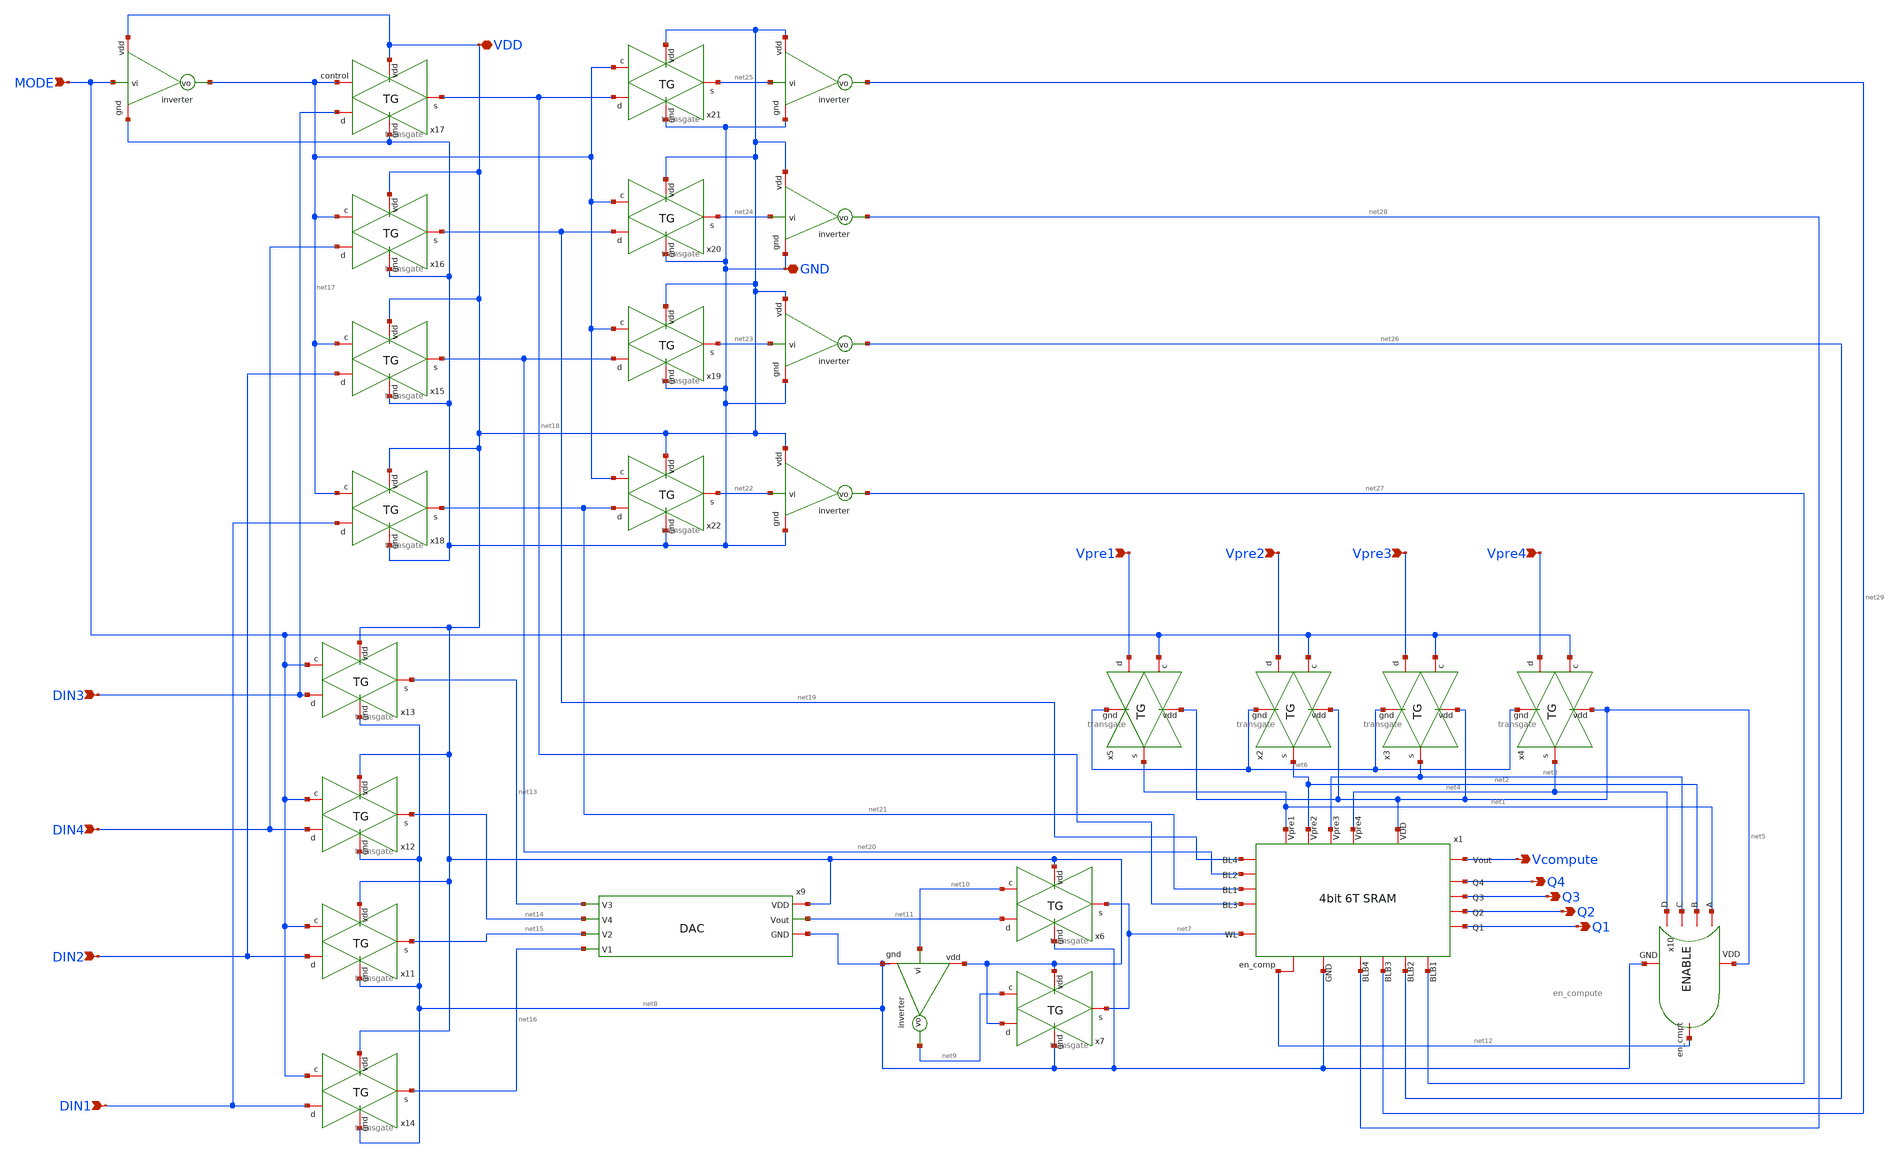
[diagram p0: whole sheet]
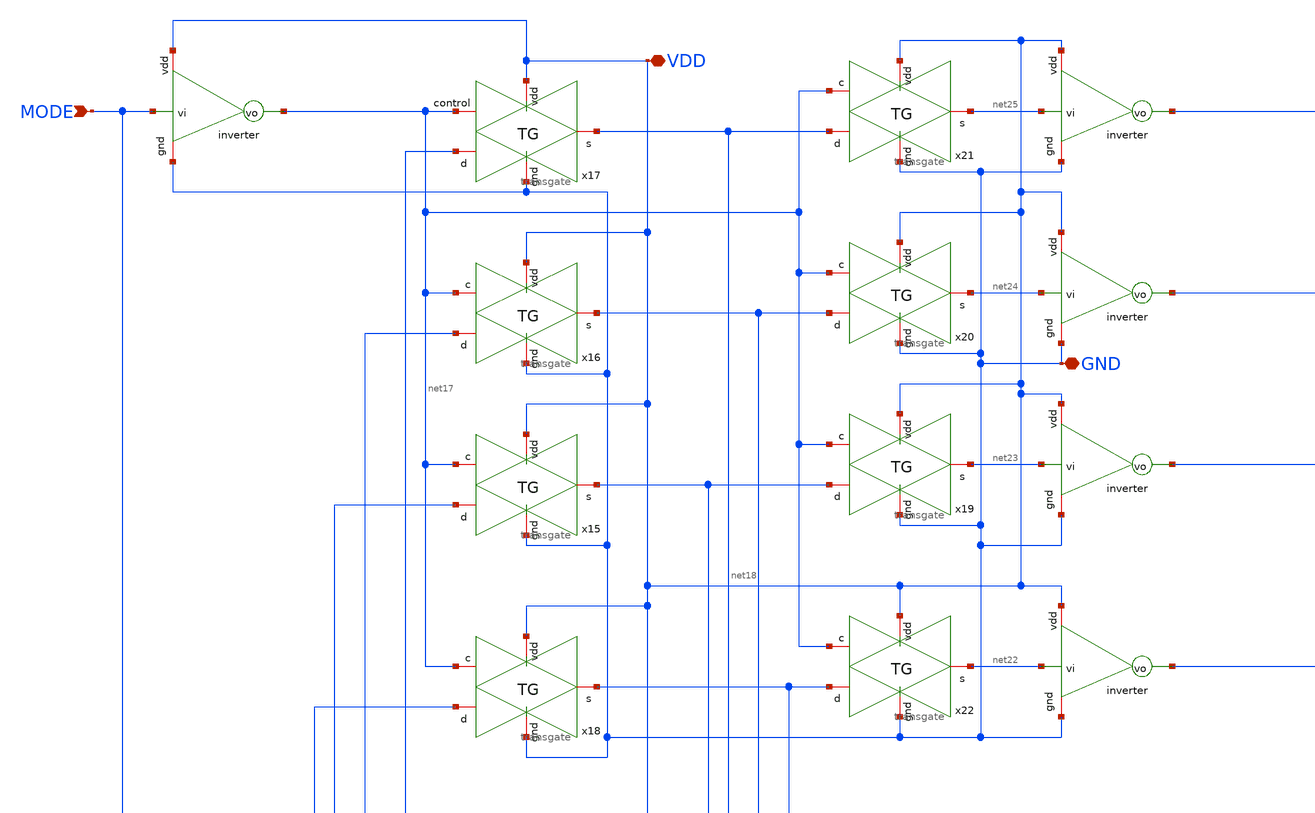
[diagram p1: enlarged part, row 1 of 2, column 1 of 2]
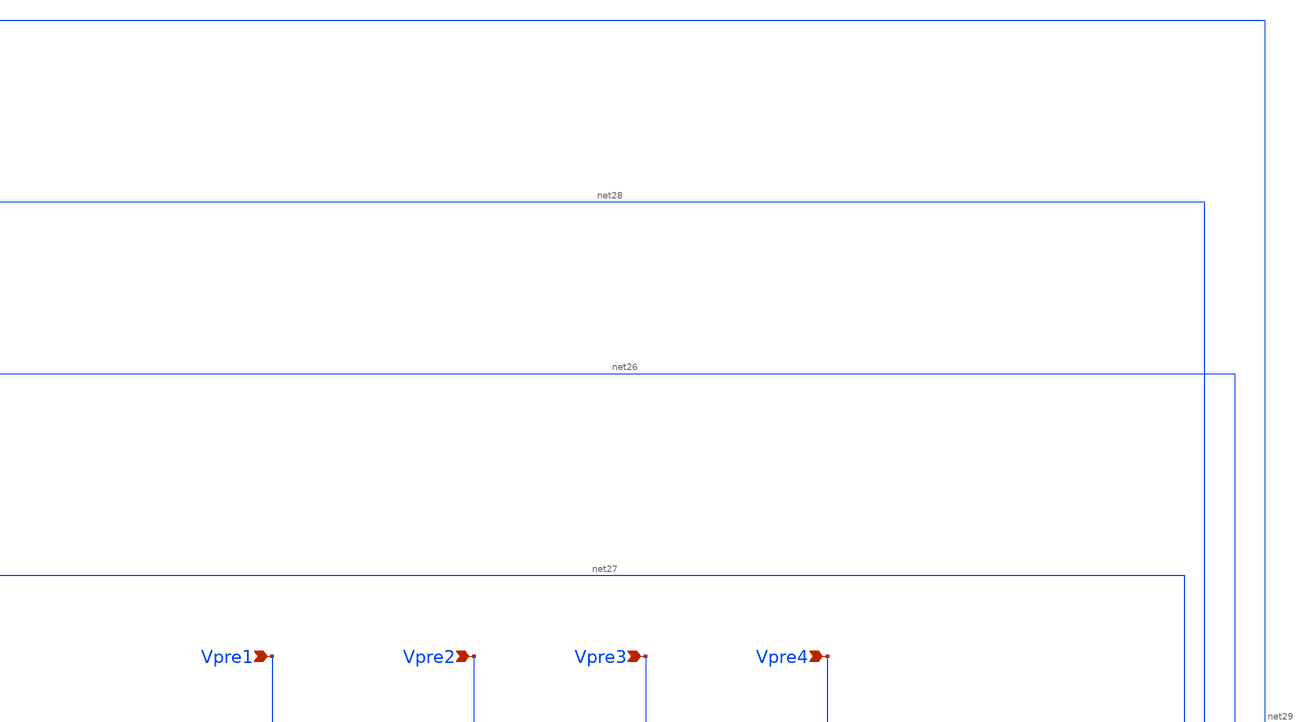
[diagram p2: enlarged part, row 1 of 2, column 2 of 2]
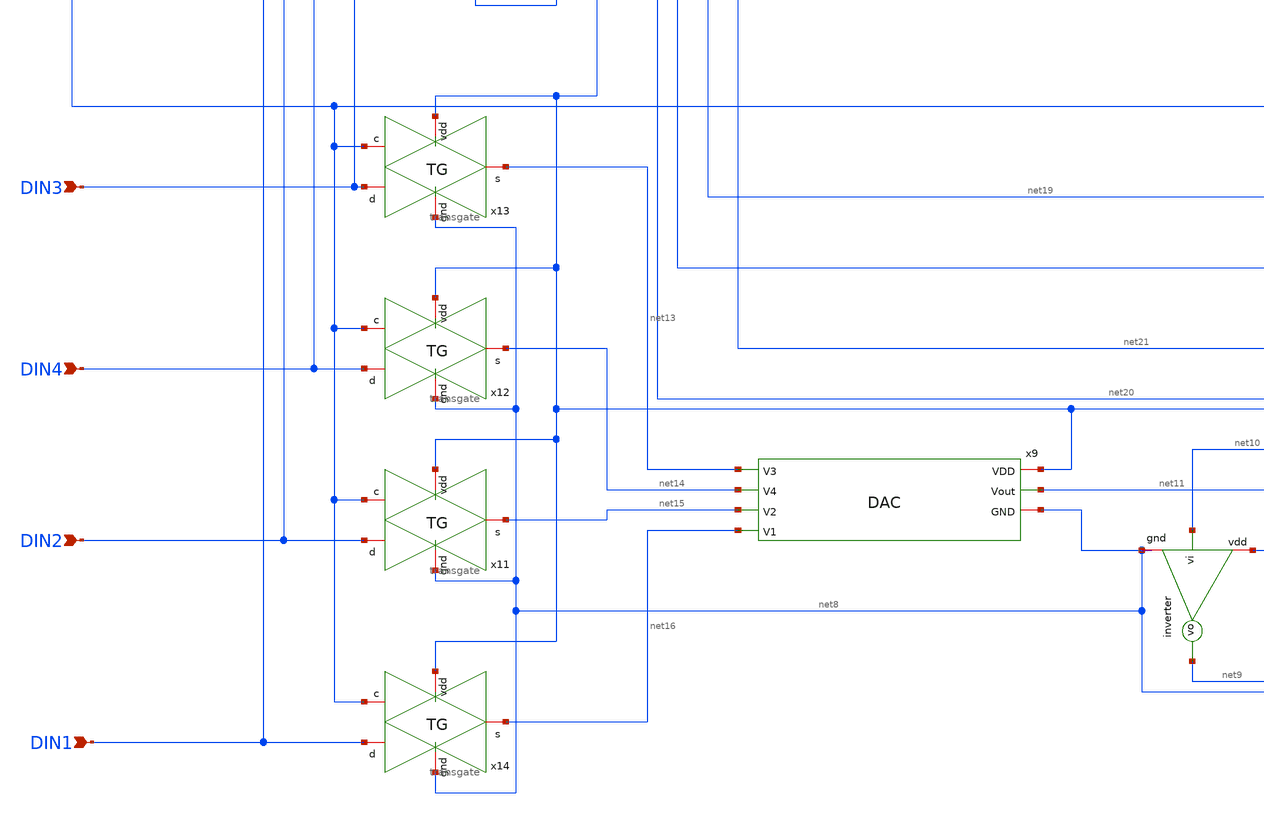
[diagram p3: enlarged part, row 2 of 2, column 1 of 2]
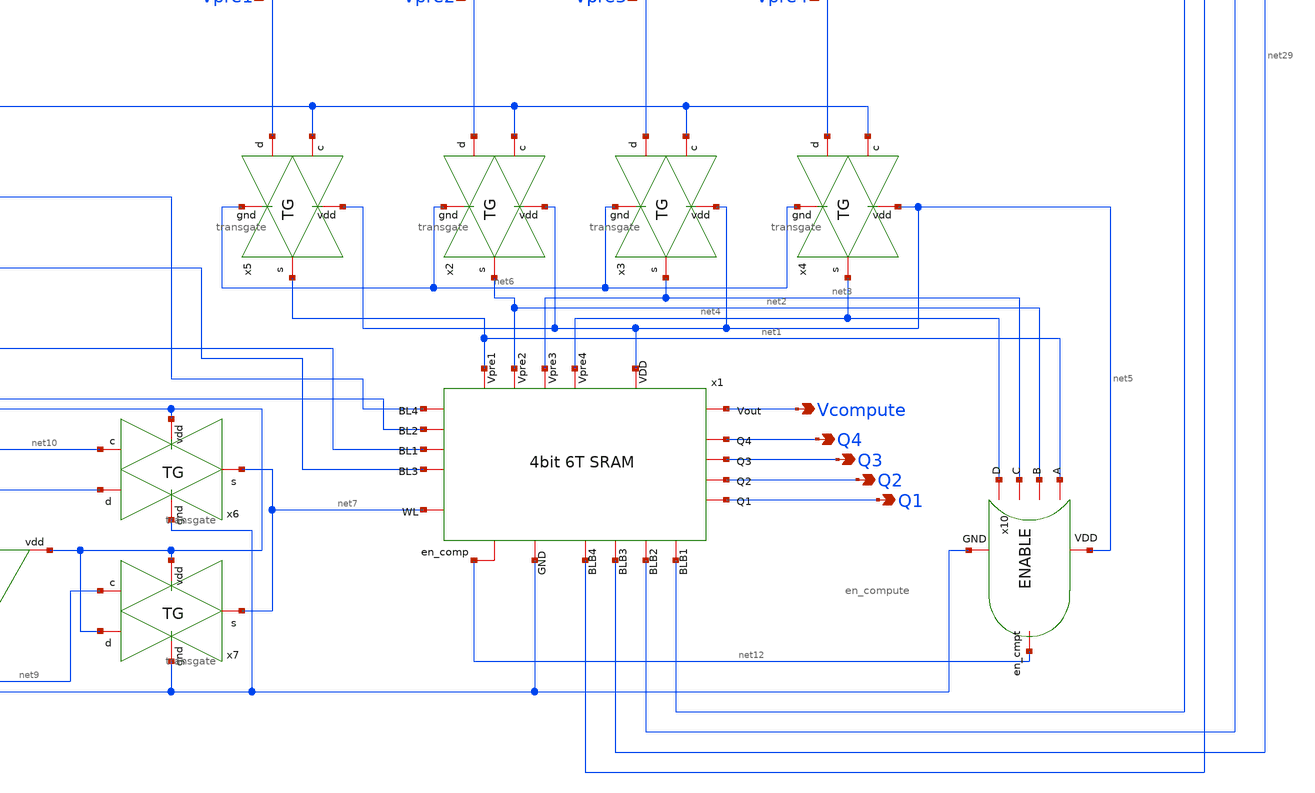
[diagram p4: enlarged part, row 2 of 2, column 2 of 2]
** sch_path: src/schematic/INTEGRASI/integrasi.sch
**.subckt integrasi Vpre1 Vpre2 Vpre3 Vpre4 DIN4 DIN3 DIN2 DIN1 MODE VDD GND Vcompute Q4 Q3 Q2 Q1
*.ipin Vpre1
*.ipin Vpre2
*.ipin Vpre3
*.ipin Vpre4
*.ipin DIN4
*.ipin DIN3
*.ipin DIN2
*.ipin DIN1
*.ipin MODE
*.iopin VDD
*.iopin GND
*.opin Vcompute
*.opin Q4
*.opin Q3
*.opin Q2
*.opin Q1
x1 net1 net2 net4 net3 net19 net20 net21 net18 net5 net7 net27 net26 net28 net29 Q4 Q3 Q2 Q1 net8
+ net12 Vcompute memori
x2 net5 net2 Vpre2 net6 MODE transgate
x3 net5 net3 Vpre3 net6 MODE transgate
x4 net5 net4 Vpre4 net6 MODE transgate
x5 net5 net1 Vpre1 net6 MODE transgate
x6 VDD net7 net11 net8 net10 transgate
x7 VDD net7 VDD net8 net9 transgate
x8 VDD net10 net9 net8 inverter
x9 VDD net11 net8 net13 net14 net15 net16 dac
x10 net5 net1 net12 net2 net3 net4 net8 en_compute
x11 VDD net15 DIN2 net8 MODE transgate
x12 VDD net14 DIN4 net8 MODE transgate
x13 VDD net13 DIN3 net8 MODE transgate
x14 VDD net16 DIN1 net8 MODE transgate
x15 VDD net20 DIN2 GND net17 transgate
x16 VDD net19 DIN4 GND net17 transgate
x17 VDD net18 DIN3 GND net17 transgate
x18 VDD net21 DIN1 GND net17 transgate
x19 VDD net23 net20 GND net17 transgate
x20 VDD net24 net19 GND net17 transgate
x21 VDD net25 net18 GND net17 transgate
x22 VDD net22 net21 GND net17 transgate
x27 VDD MODE net17 GND inverter
x23 VDD net25 net29 GND inverter
x24 VDD net24 net28 GND inverter
x25 VDD net23 net26 GND inverter
x26 VDD net22 net27 GND inverter
**.ends
.end
